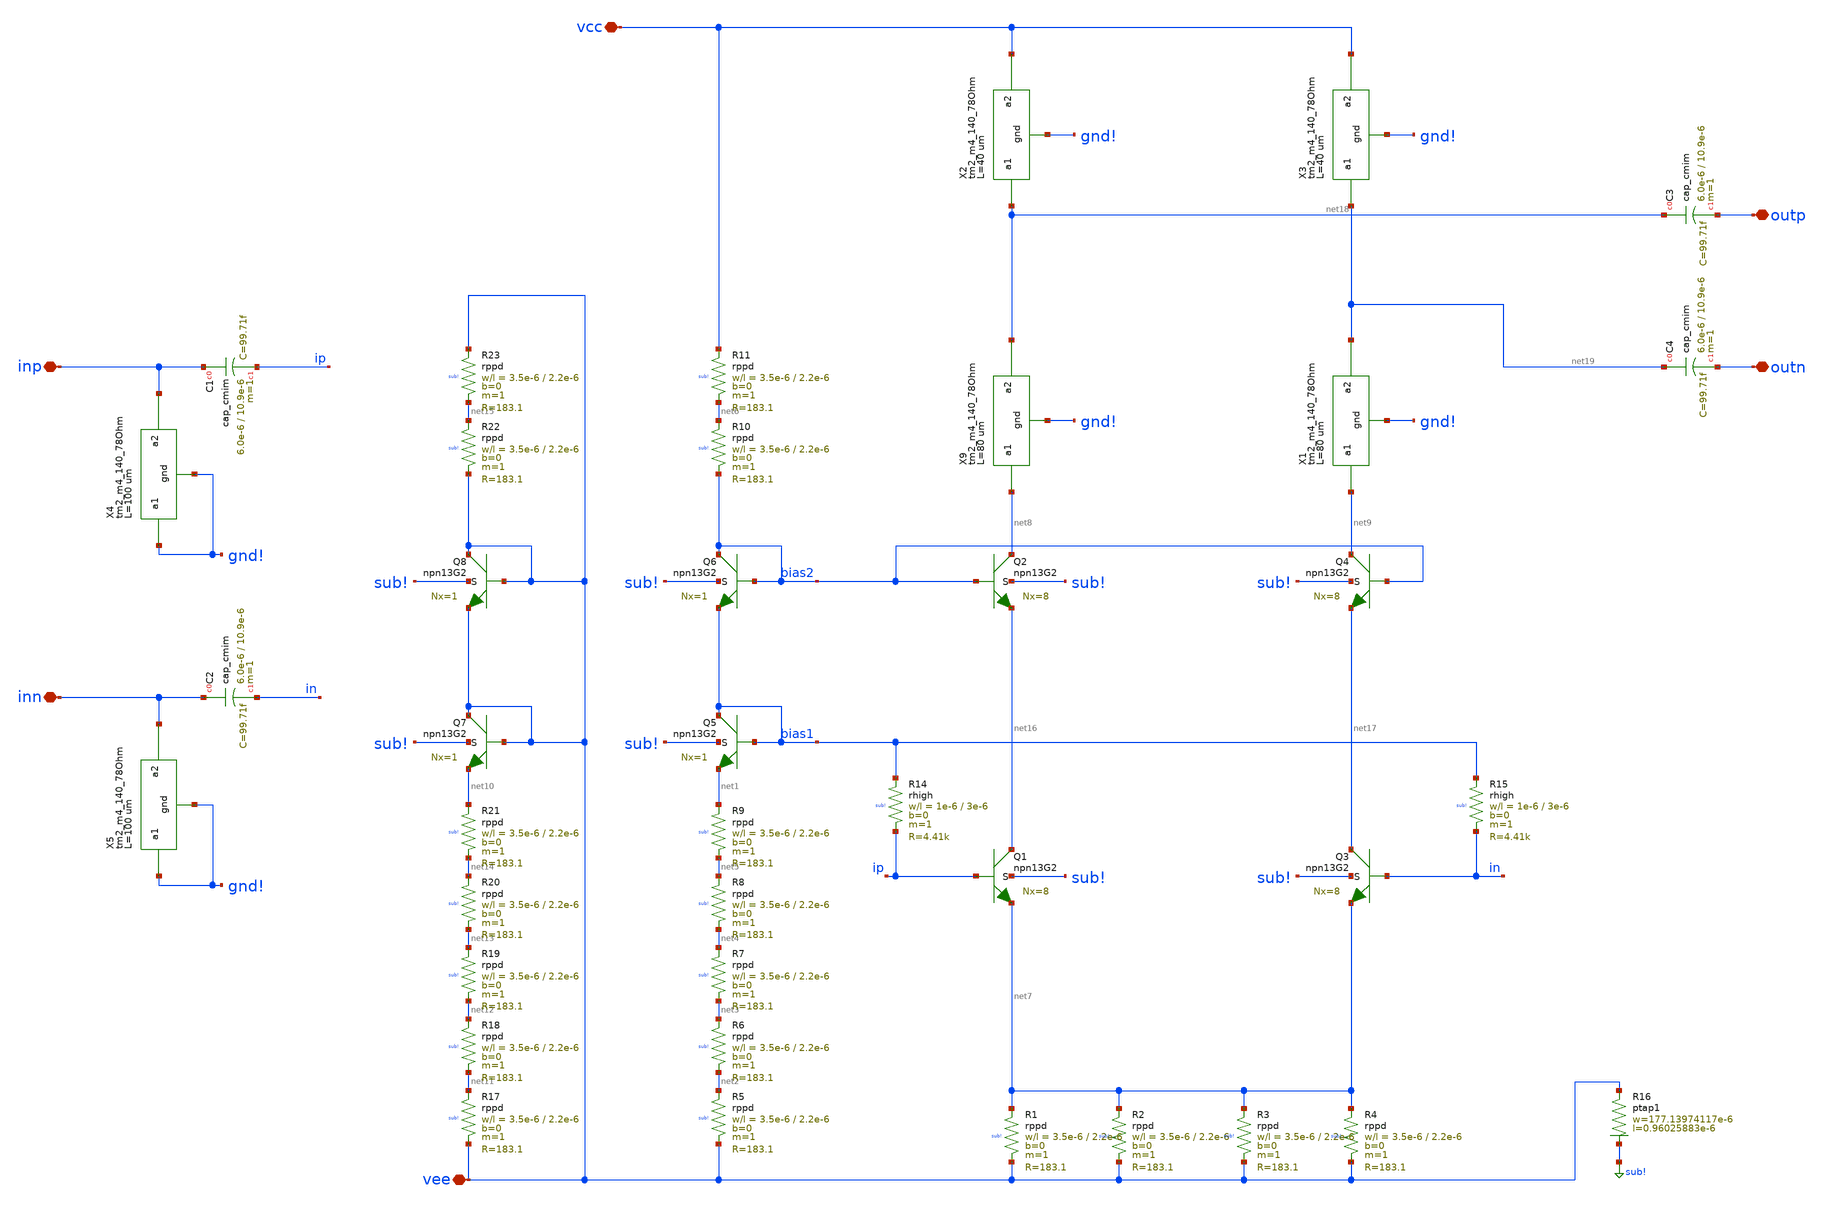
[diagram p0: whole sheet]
** sch_path: LNA0379-main/schematic/xschem/LNA0379_coreTL.sch
**.subckt LNA0379_coreTL inp inn vcc vee outp outn
*.iopin inp
*.iopin inn
*.iopin vcc
*.iopin vee
*.iopin outp
*.iopin outn
XQ1 net16 ip net7 sub! npn13G2 Nx=8 mm_ok=1
XQ2 net8 bias2 net16 sub! npn13G2 Nx=8 mm_ok=1
XQ3 net17 in net7 sub! npn13G2 Nx=8 mm_ok=1
XQ4 net9 bias2 net17 sub! npn13G2 Nx=8 mm_ok=1
XQ5 bias1 bias1 net1 sub! npn13G2 Nx=1 mm_ok=1
XQ6 bias2 bias2 bias1 sub! npn13G2 Nx=1 mm_ok=1
XR14 bias1 ip sub! rhigh w=1e-6 l=3e-6 m=1 b=0 mm_ok=1
XR15 bias1 in sub! rhigh w=1e-6 l=3e-6 m=1 b=0 mm_ok=1
XR1 net7 vee sub! rppd w=3.5e-6 l=2.2e-6 m=1 b=0 mm_ok=1
XR16 vee sub! ptap1 R=1.862 w=177.13974117e-6 l=0.96025883e-6
XQ7 vee vee net10 sub! npn13G2 Nx=1 mm_ok=1
XQ8 vee vee vee sub! npn13G2 Nx=1 mm_ok=1
XR2 net7 vee sub! rppd w=3.5e-6 l=2.2e-6 m=1 b=0 mm_ok=1
XR3 net7 vee sub! rppd w=3.5e-6 l=2.2e-6 m=1 b=0 mm_ok=1
XR4 net7 vee sub! rppd w=3.5e-6 l=2.2e-6 m=1 b=0 mm_ok=1
XR5 net2 vee sub! rppd w=3.5e-6 l=2.2e-6 m=1 b=0 mm_ok=1
XR6 net3 net2 sub! rppd w=3.5e-6 l=2.2e-6 m=1 b=0 mm_ok=1
XR7 net4 net3 sub! rppd w=3.5e-6 l=2.2e-6 m=1 b=0 mm_ok=1
XR8 net5 net4 sub! rppd w=3.5e-6 l=2.2e-6 m=1 b=0 mm_ok=1
XR9 net1 net5 sub! rppd w=3.5e-6 l=2.2e-6 m=1 b=0 mm_ok=1
XR10 net6 bias2 sub! rppd w=3.5e-6 l=2.2e-6 m=1 b=0 mm_ok=1
XR11 vcc net6 sub! rppd w=3.5e-6 l=2.2e-6 m=1 b=0 mm_ok=1
XR17 net11 vee sub! rppd w=3.5e-6 l=2.2e-6 m=1 b=0 mm_ok=1
XR18 net12 net11 sub! rppd w=3.5e-6 l=2.2e-6 m=1 b=0 mm_ok=1
XR19 net13 net12 sub! rppd w=3.5e-6 l=2.2e-6 m=1 b=0 mm_ok=1
XR20 net14 net13 sub! rppd w=3.5e-6 l=2.2e-6 m=1 b=0 mm_ok=1
XR21 net10 net14 sub! rppd w=3.5e-6 l=2.2e-6 m=1 b=0 mm_ok=1
XR22 net15 vee sub! rppd w=3.5e-6 l=2.2e-6 m=1 b=0 mm_ok=1
XR23 vee net15 sub! rppd w=3.5e-6 l=2.2e-6 m=1 b=0 mm_ok=1
XC1 inp ip cap_cmim w=6.0e-6 l=10.9e-6 m=1 mm_ok=1
XC2 inn in cap_cmim w=6.0e-6 l=10.9e-6 m=1 mm_ok=1
XC3 net18 outp cap_cmim w=6.0e-6 l=10.9e-6 m=1 mm_ok=1
XC4 net19 outn cap_cmim w=6.0e-6 l=10.9e-6 m=1 mm_ok=1
XX9 net8 net18 gnd! tm2_m4_140_78Ohm length_um=80
XX1 net9 net19 gnd! tm2_m4_140_78Ohm length_um=80
XX2 net18 vcc gnd! tm2_m4_140_78Ohm length_um=40
XX3 net19 vcc gnd! tm2_m4_140_78Ohm length_um=40
XX4 gnd! inp gnd! tm2_m4_140_78Ohm length_um=100
XX5 gnd! inn gnd! tm2_m4_140_78Ohm length_um=100
**.ends
.GLOBAL sub!
.end
